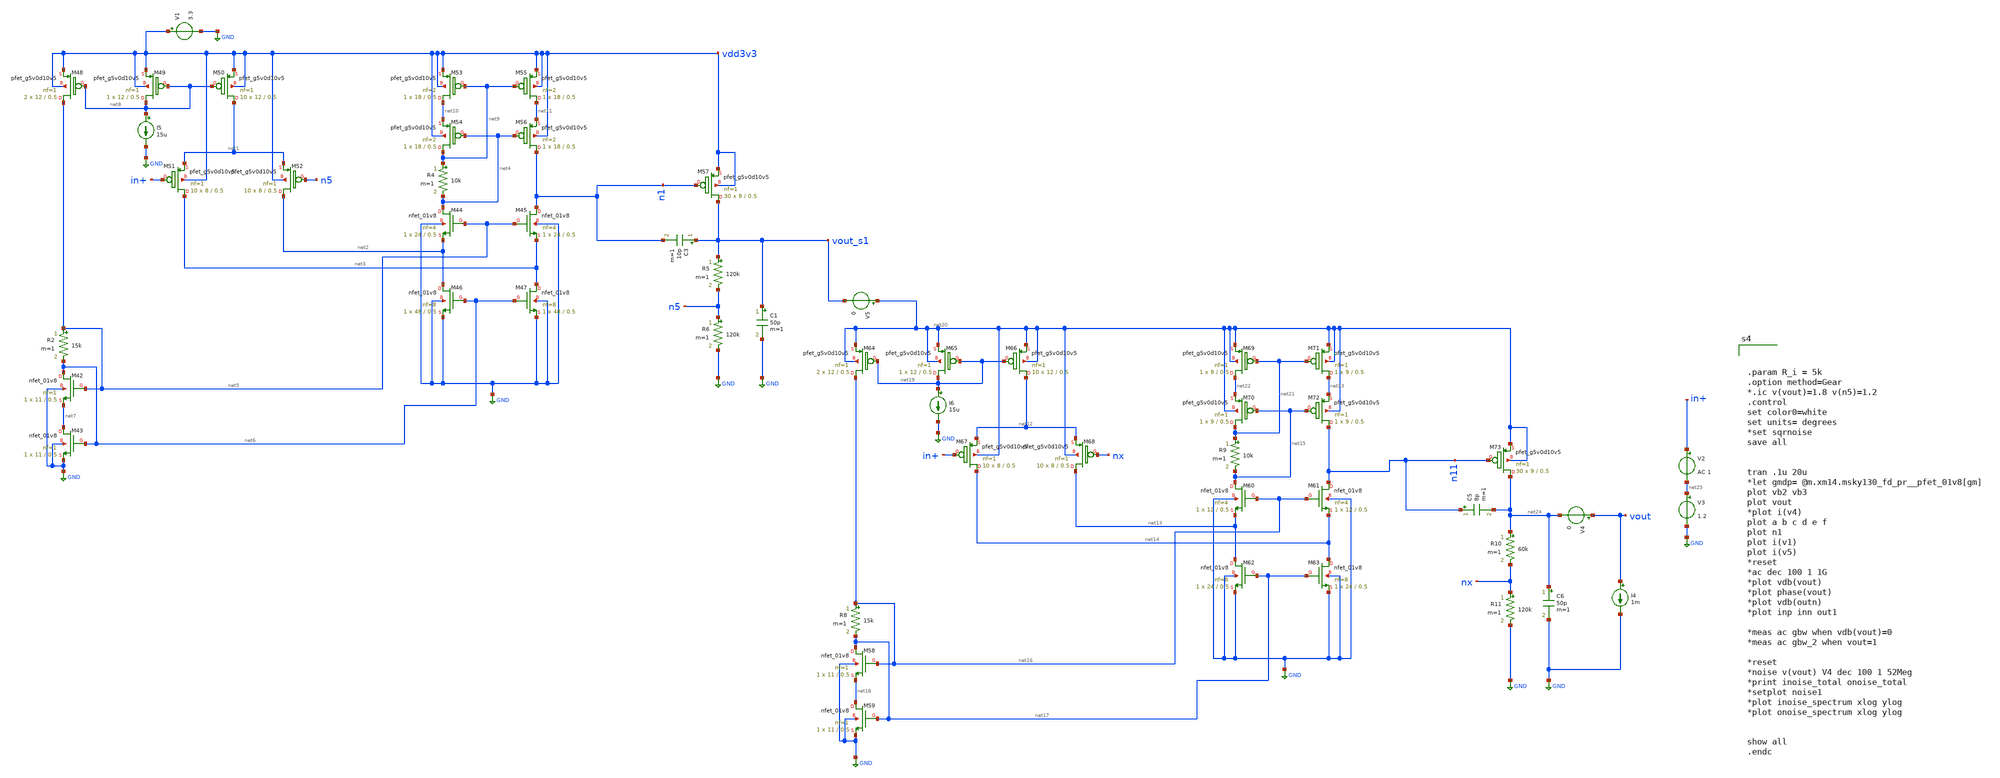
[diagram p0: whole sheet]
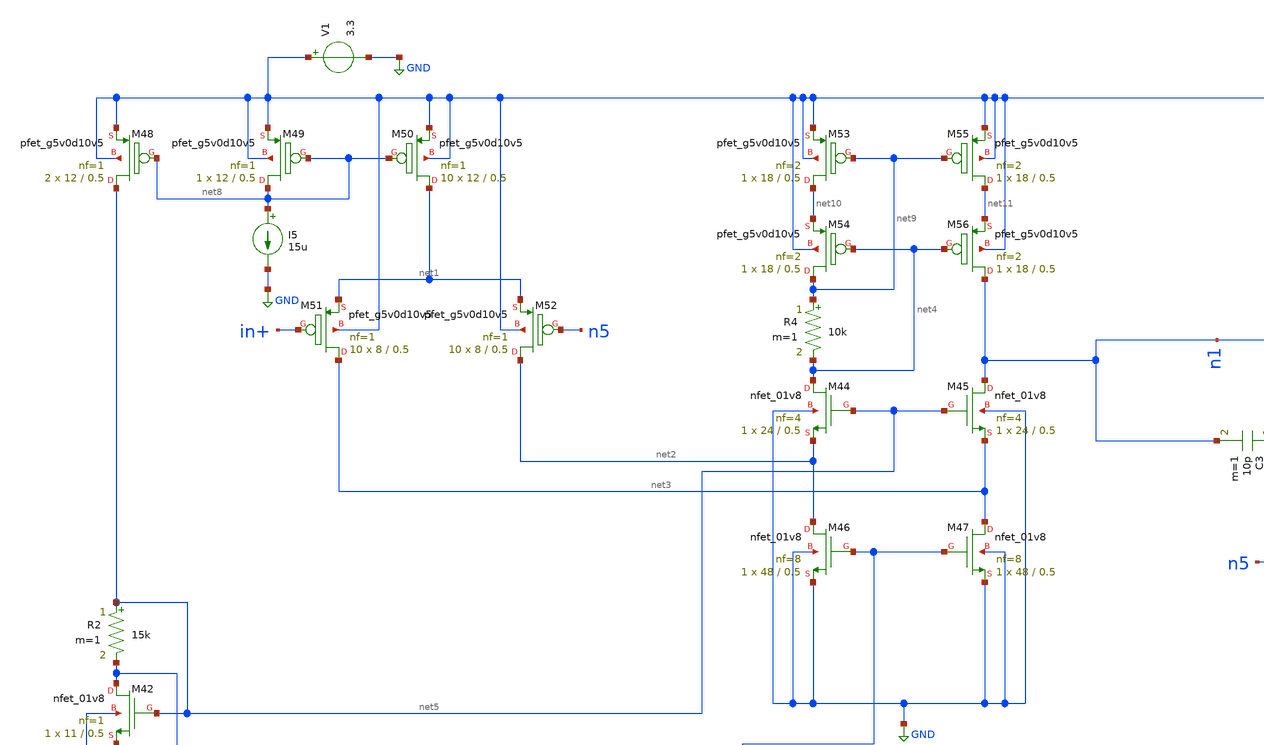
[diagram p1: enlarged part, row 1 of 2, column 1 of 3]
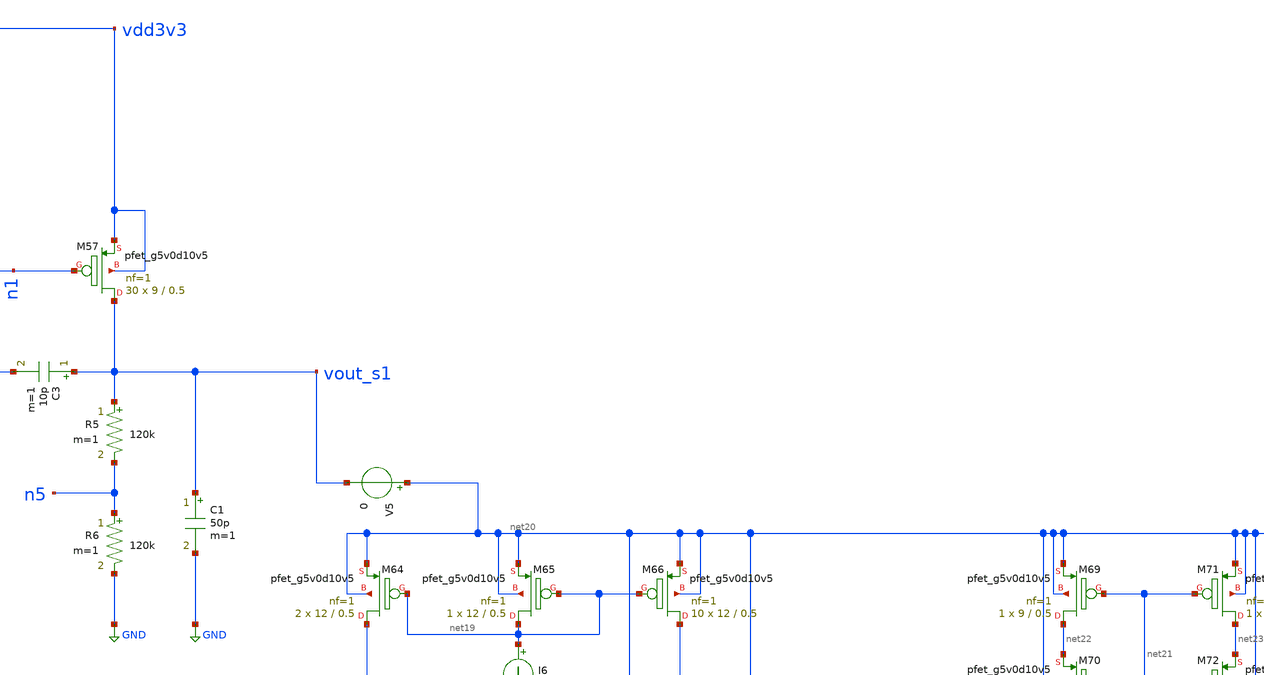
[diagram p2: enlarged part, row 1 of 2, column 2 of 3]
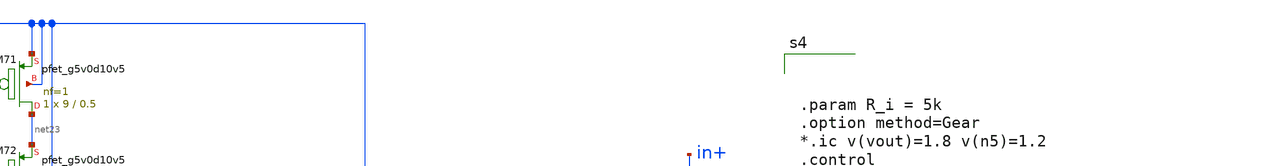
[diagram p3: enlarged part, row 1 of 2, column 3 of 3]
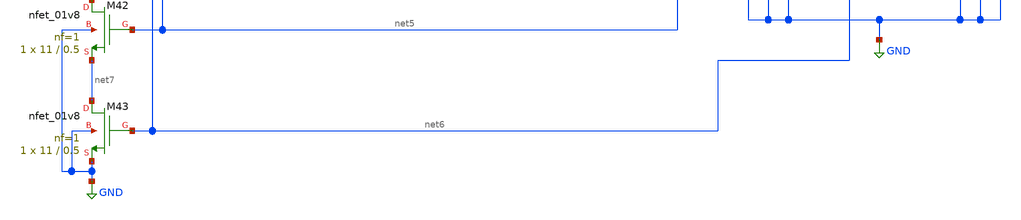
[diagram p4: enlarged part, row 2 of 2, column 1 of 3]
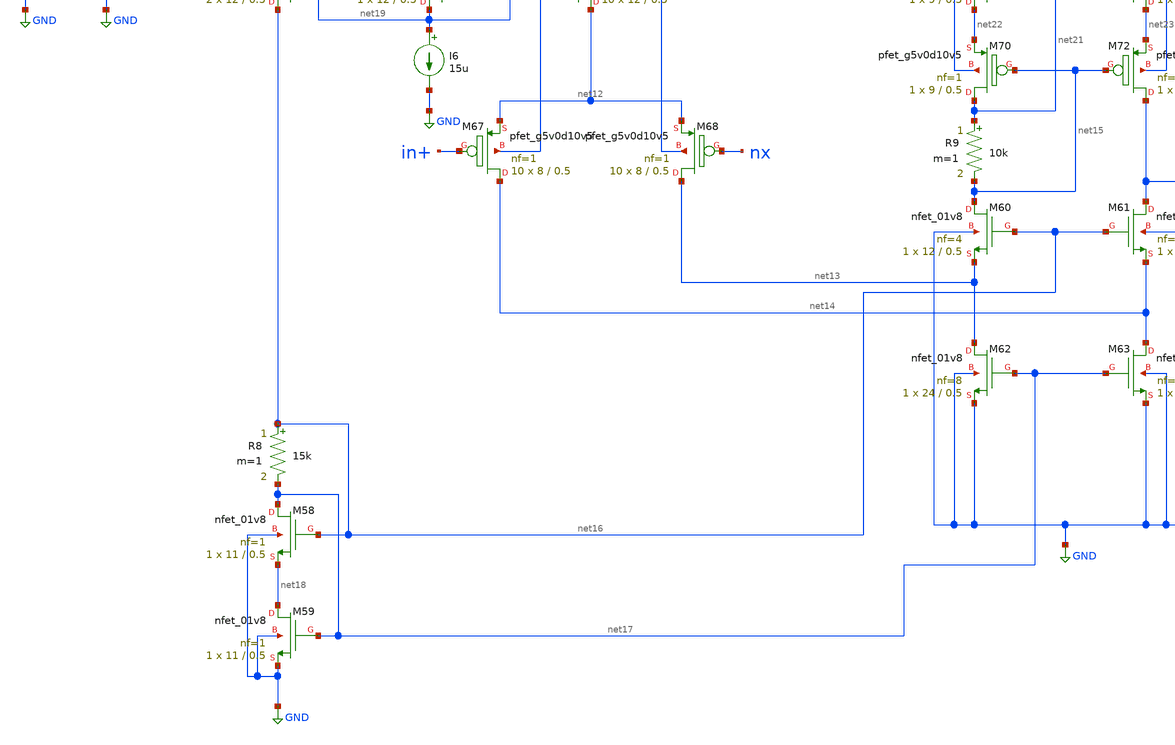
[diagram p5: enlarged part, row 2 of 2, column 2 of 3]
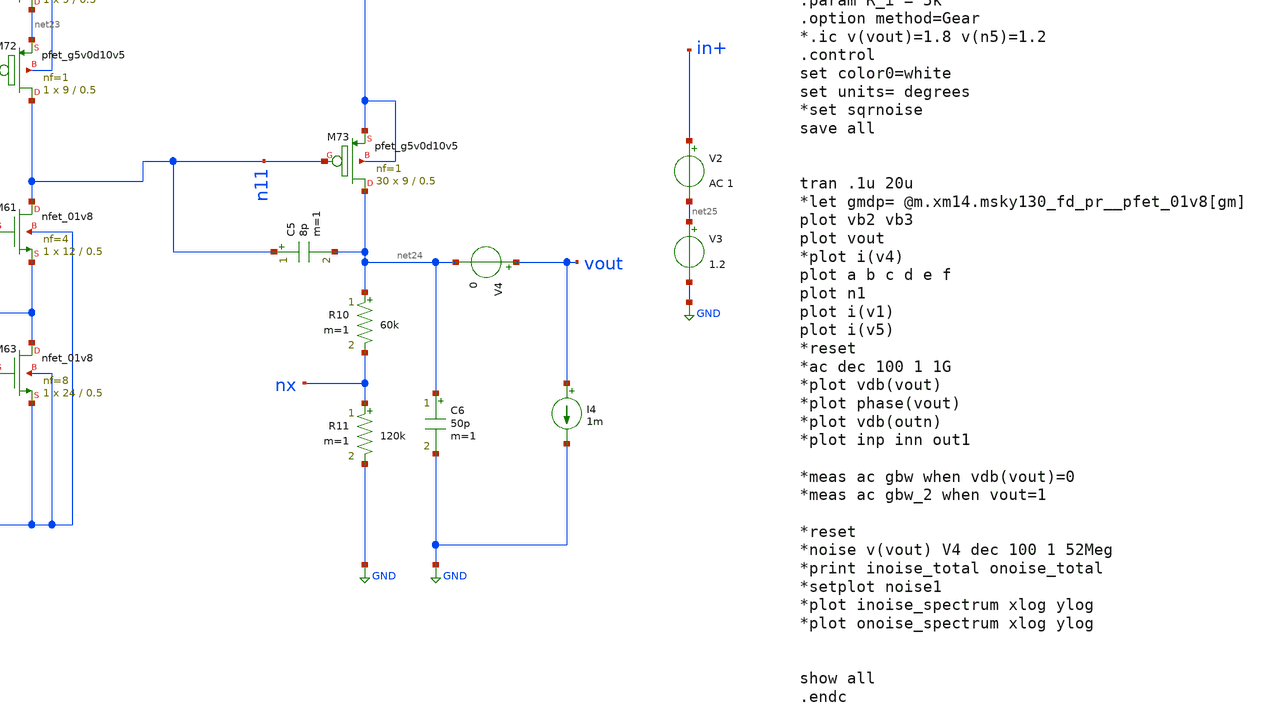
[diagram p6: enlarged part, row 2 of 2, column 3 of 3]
** sch_path: analog/analog_ldo/ceyda_src/cascade_ldo_tran.sch
**.subckt cascade_ldo_tran
R2 net5 net6 15k m=1
I5 net8 GND 15u
V1 vdd3v3 GND 3.3
R4 net9 net4 10k m=1
XM42 net6 net5 net7 GND sky130_fd_pr__nfet_01v8 L=0.5 W=11 nf=1 ad='int((nf+1)/2) * W/nf * 0.29' as='int((nf+2)/2) * W/nf * 0.29'
+ pd='2*int((nf+1)/2) * (W/nf + 0.29)' ps='2*int((nf+2)/2) * (W/nf + 0.29)' nrd='0.29 / W' nrs='0.29 / W'
+ sa=0 sb=0 sd=0 mult=1 m=1
XM43 net7 net6 GND GND sky130_fd_pr__nfet_01v8 L=0.5 W=11 nf=1 ad='int((nf+1)/2) * W/nf * 0.29' as='int((nf+2)/2) * W/nf * 0.29'
+ pd='2*int((nf+1)/2) * (W/nf + 0.29)' ps='2*int((nf+2)/2) * (W/nf + 0.29)' nrd='0.29 / W' nrs='0.29 / W'
+ sa=0 sb=0 sd=0 mult=1 m=1
XM44 net4 net5 net2 GND sky130_fd_pr__nfet_01v8 L=0.5 W=24 nf=4 ad='int((nf+1)/2) * W/nf * 0.29' as='int((nf+2)/2) * W/nf * 0.29'
+ pd='2*int((nf+1)/2) * (W/nf + 0.29)' ps='2*int((nf+2)/2) * (W/nf + 0.29)' nrd='0.29 / W' nrs='0.29 / W'
+ sa=0 sb=0 sd=0 mult=1 m=1
XM45 n1 net5 net3 GND sky130_fd_pr__nfet_01v8 L=0.5 W=24 nf=4 ad='int((nf+1)/2) * W/nf * 0.29' as='int((nf+2)/2) * W/nf * 0.29'
+ pd='2*int((nf+1)/2) * (W/nf + 0.29)' ps='2*int((nf+2)/2) * (W/nf + 0.29)' nrd='0.29 / W' nrs='0.29 / W'
+ sa=0 sb=0 sd=0 mult=1 m=1
XM46 net2 net6 GND GND sky130_fd_pr__nfet_01v8 L=0.5 W=48 nf=8 ad='int((nf+1)/2) * W/nf * 0.29' as='int((nf+2)/2) * W/nf * 0.29'
+ pd='2*int((nf+1)/2) * (W/nf + 0.29)' ps='2*int((nf+2)/2) * (W/nf + 0.29)' nrd='0.29 / W' nrs='0.29 / W'
+ sa=0 sb=0 sd=0 mult=1 m=1
XM47 net3 net6 GND GND sky130_fd_pr__nfet_01v8 L=0.5 W=48 nf=8 ad='int((nf+1)/2) * W/nf * 0.29' as='int((nf+2)/2) * W/nf * 0.29'
+ pd='2*int((nf+1)/2) * (W/nf + 0.29)' ps='2*int((nf+2)/2) * (W/nf + 0.29)' nrd='0.29 / W' nrs='0.29 / W'
+ sa=0 sb=0 sd=0 mult=1 m=1
XM48 net5 net8 vdd3v3 vdd3v3 sky130_fd_pr__pfet_g5v0d10v5 L=0.5 W=12 nf=1 ad='int((nf+1)/2) * W/nf * 0.29'
+ as='int((nf+2)/2) * W/nf * 0.29' pd='2*int((nf+1)/2) * (W/nf + 0.29)' ps='2*int((nf+2)/2) * (W/nf + 0.29)'
+ nrd='0.29 / W' nrs='0.29 / W' sa=0 sb=0 sd=0 mult=2 m=2
XM49 net8 net8 vdd3v3 vdd3v3 sky130_fd_pr__pfet_g5v0d10v5 L=0.5 W=12 nf=1 ad='int((nf+1)/2) * W/nf * 0.29'
+ as='int((nf+2)/2) * W/nf * 0.29' pd='2*int((nf+1)/2) * (W/nf + 0.29)' ps='2*int((nf+2)/2) * (W/nf + 0.29)'
+ nrd='0.29 / W' nrs='0.29 / W' sa=0 sb=0 sd=0 mult=1 m=1
XM50 net1 net8 vdd3v3 vdd3v3 sky130_fd_pr__pfet_g5v0d10v5 L=0.5 W=12 nf=1 ad='int((nf+1)/2) * W/nf * 0.29'
+ as='int((nf+2)/2) * W/nf * 0.29' pd='2*int((nf+1)/2) * (W/nf + 0.29)' ps='2*int((nf+2)/2) * (W/nf + 0.29)'
+ nrd='0.29 / W' nrs='0.29 / W' sa=0 sb=0 sd=0 mult=10 m=10
XM51 net3 in+ net1 vdd3v3 sky130_fd_pr__pfet_g5v0d10v5 L=0.5 W=8 nf=1 ad='int((nf+1)/2) * W/nf * 0.29'
+ as='int((nf+2)/2) * W/nf * 0.29' pd='2*int((nf+1)/2) * (W/nf + 0.29)' ps='2*int((nf+2)/2) * (W/nf + 0.29)'
+ nrd='0.29 / W' nrs='0.29 / W' sa=0 sb=0 sd=0 mult=10 m=10
XM52 net2 n5 net1 vdd3v3 sky130_fd_pr__pfet_g5v0d10v5 L=0.5 W=8 nf=1 ad='int((nf+1)/2) * W/nf * 0.29'
+ as='int((nf+2)/2) * W/nf * 0.29' pd='2*int((nf+1)/2) * (W/nf + 0.29)' ps='2*int((nf+2)/2) * (W/nf + 0.29)'
+ nrd='0.29 / W' nrs='0.29 / W' sa=0 sb=0 sd=0 mult=10 m=10
XM53 net10 net9 vdd3v3 vdd3v3 sky130_fd_pr__pfet_g5v0d10v5 L=0.5 W=18 nf=2 ad='int((nf+1)/2) * W/nf * 0.29'
+ as='int((nf+2)/2) * W/nf * 0.29' pd='2*int((nf+1)/2) * (W/nf + 0.29)' ps='2*int((nf+2)/2) * (W/nf + 0.29)'
+ nrd='0.29 / W' nrs='0.29 / W' sa=0 sb=0 sd=0 mult=1 m=1
XM54 net9 net4 net10 vdd3v3 sky130_fd_pr__pfet_g5v0d10v5 L=0.5 W=18 nf=2 ad='int((nf+1)/2) * W/nf * 0.29'
+ as='int((nf+2)/2) * W/nf * 0.29' pd='2*int((nf+1)/2) * (W/nf + 0.29)' ps='2*int((nf+2)/2) * (W/nf + 0.29)'
+ nrd='0.29 / W' nrs='0.29 / W' sa=0 sb=0 sd=0 mult=1 m=1
XM55 net11 net9 vdd3v3 vdd3v3 sky130_fd_pr__pfet_g5v0d10v5 L=0.5 W=18 nf=2 ad='int((nf+1)/2) * W/nf * 0.29'
+ as='int((nf+2)/2) * W/nf * 0.29' pd='2*int((nf+1)/2) * (W/nf + 0.29)' ps='2*int((nf+2)/2) * (W/nf + 0.29)'
+ nrd='0.29 / W' nrs='0.29 / W' sa=0 sb=0 sd=0 mult=1 m=1
XM56 n1 net4 net11 vdd3v3 sky130_fd_pr__pfet_g5v0d10v5 L=0.5 W=18 nf=2 ad='int((nf+1)/2) * W/nf * 0.29'
+ as='int((nf+2)/2) * W/nf * 0.29' pd='2*int((nf+1)/2) * (W/nf + 0.29)' ps='2*int((nf+2)/2) * (W/nf + 0.29)'
+ nrd='0.29 / W' nrs='0.29 / W' sa=0 sb=0 sd=0 mult=1 m=1
R5 vout_s1 n5 120k m=1
R6 n5 GND 120k m=1
XM57 vout_s1 n1 vdd3v3 vdd3v3 sky130_fd_pr__pfet_g5v0d10v5 L=0.5 W=9 nf=1 ad='int((nf+1)/2) * W/nf * 0.29'
+ as='int((nf+2)/2) * W/nf * 0.29' pd='2*int((nf+1)/2) * (W/nf + 0.29)' ps='2*int((nf+2)/2) * (W/nf + 0.29)'
+ nrd='0.29 / W' nrs='0.29 / W' sa=0 sb=0 sd=0 mult=30 m=30
R8 net16 net17 15k m=1
I6 net19 GND 15u
R9 net21 net15 10k m=1
XM58 net17 net16 net18 GND sky130_fd_pr__nfet_01v8 L=0.5 W=11 nf=1 ad='int((nf+1)/2) * W/nf * 0.29' as='int((nf+2)/2) * W/nf * 0.29'
+ pd='2*int((nf+1)/2) * (W/nf + 0.29)' ps='2*int((nf+2)/2) * (W/nf + 0.29)' nrd='0.29 / W' nrs='0.29 / W'
+ sa=0 sb=0 sd=0 mult=1 m=1
XM59 net18 net17 GND GND sky130_fd_pr__nfet_01v8 L=0.5 W=11 nf=1 ad='int((nf+1)/2) * W/nf * 0.29' as='int((nf+2)/2) * W/nf * 0.29'
+ pd='2*int((nf+1)/2) * (W/nf + 0.29)' ps='2*int((nf+2)/2) * (W/nf + 0.29)' nrd='0.29 / W' nrs='0.29 / W'
+ sa=0 sb=0 sd=0 mult=1 m=1
XM60 net15 net16 net13 GND sky130_fd_pr__nfet_01v8 L=0.5 W=12 nf=4 ad='int((nf+1)/2) * W/nf * 0.29' as='int((nf+2)/2) * W/nf * 0.29'
+ pd='2*int((nf+1)/2) * (W/nf + 0.29)' ps='2*int((nf+2)/2) * (W/nf + 0.29)' nrd='0.29 / W' nrs='0.29 / W'
+ sa=0 sb=0 sd=0 mult=1 m=1
XM61 n11 net16 net14 GND sky130_fd_pr__nfet_01v8 L=0.5 W=12 nf=4 ad='int((nf+1)/2) * W/nf * 0.29' as='int((nf+2)/2) * W/nf * 0.29'
+ pd='2*int((nf+1)/2) * (W/nf + 0.29)' ps='2*int((nf+2)/2) * (W/nf + 0.29)' nrd='0.29 / W' nrs='0.29 / W'
+ sa=0 sb=0 sd=0 mult=1 m=1
XM62 net13 net17 GND GND sky130_fd_pr__nfet_01v8 L=0.5 W=24 nf=8 ad='int((nf+1)/2) * W/nf * 0.29' as='int((nf+2)/2) * W/nf * 0.29'
+ pd='2*int((nf+1)/2) * (W/nf + 0.29)' ps='2*int((nf+2)/2) * (W/nf + 0.29)' nrd='0.29 / W' nrs='0.29 / W'
+ sa=0 sb=0 sd=0 mult=1 m=1
XM63 net14 net17 GND GND sky130_fd_pr__nfet_01v8 L=0.5 W=24 nf=8 ad='int((nf+1)/2) * W/nf * 0.29' as='int((nf+2)/2) * W/nf * 0.29'
+ pd='2*int((nf+1)/2) * (W/nf + 0.29)' ps='2*int((nf+2)/2) * (W/nf + 0.29)' nrd='0.29 / W' nrs='0.29 / W'
+ sa=0 sb=0 sd=0 mult=1 m=1
XM64 net16 net19 net20 net20 sky130_fd_pr__pfet_g5v0d10v5 L=0.5 W=12 nf=1 ad='int((nf+1)/2) * W/nf * 0.29'
+ as='int((nf+2)/2) * W/nf * 0.29' pd='2*int((nf+1)/2) * (W/nf + 0.29)' ps='2*int((nf+2)/2) * (W/nf + 0.29)'
+ nrd='0.29 / W' nrs='0.29 / W' sa=0 sb=0 sd=0 mult=2 m=2
XM65 net19 net19 net20 net20 sky130_fd_pr__pfet_g5v0d10v5 L=0.5 W=12 nf=1 ad='int((nf+1)/2) * W/nf * 0.29'
+ as='int((nf+2)/2) * W/nf * 0.29' pd='2*int((nf+1)/2) * (W/nf + 0.29)' ps='2*int((nf+2)/2) * (W/nf + 0.29)'
+ nrd='0.29 / W' nrs='0.29 / W' sa=0 sb=0 sd=0 mult=1 m=1
XM66 net12 net19 net20 net20 sky130_fd_pr__pfet_g5v0d10v5 L=0.5 W=12 nf=1 ad='int((nf+1)/2) * W/nf * 0.29'
+ as='int((nf+2)/2) * W/nf * 0.29' pd='2*int((nf+1)/2) * (W/nf + 0.29)' ps='2*int((nf+2)/2) * (W/nf + 0.29)'
+ nrd='0.29 / W' nrs='0.29 / W' sa=0 sb=0 sd=0 mult=10 m=10
XM67 net14 in+ net12 net20 sky130_fd_pr__pfet_g5v0d10v5 L=0.5 W=8 nf=1 ad='int((nf+1)/2) * W/nf * 0.29'
+ as='int((nf+2)/2) * W/nf * 0.29' pd='2*int((nf+1)/2) * (W/nf + 0.29)' ps='2*int((nf+2)/2) * (W/nf + 0.29)'
+ nrd='0.29 / W' nrs='0.29 / W' sa=0 sb=0 sd=0 mult=10 m=10
XM68 net13 nx net12 net20 sky130_fd_pr__pfet_g5v0d10v5 L=0.5 W=8 nf=1 ad='int((nf+1)/2) * W/nf * 0.29'
+ as='int((nf+2)/2) * W/nf * 0.29' pd='2*int((nf+1)/2) * (W/nf + 0.29)' ps='2*int((nf+2)/2) * (W/nf + 0.29)'
+ nrd='0.29 / W' nrs='0.29 / W' sa=0 sb=0 sd=0 mult=10 m=10
XM69 net22 net21 net20 net20 sky130_fd_pr__pfet_g5v0d10v5 L=0.5 W=9 nf=1 ad='int((nf+1)/2) * W/nf * 0.29'
+ as='int((nf+2)/2) * W/nf * 0.29' pd='2*int((nf+1)/2) * (W/nf + 0.29)' ps='2*int((nf+2)/2) * (W/nf + 0.29)'
+ nrd='0.29 / W' nrs='0.29 / W' sa=0 sb=0 sd=0 mult=1 m=1
XM70 net21 net15 net22 net20 sky130_fd_pr__pfet_g5v0d10v5 L=0.5 W=9 nf=1 ad='int((nf+1)/2) * W/nf * 0.29'
+ as='int((nf+2)/2) * W/nf * 0.29' pd='2*int((nf+1)/2) * (W/nf + 0.29)' ps='2*int((nf+2)/2) * (W/nf + 0.29)'
+ nrd='0.29 / W' nrs='0.29 / W' sa=0 sb=0 sd=0 mult=1 m=1
XM71 net23 net21 net20 net20 sky130_fd_pr__pfet_g5v0d10v5 L=0.5 W=9 nf=1 ad='int((nf+1)/2) * W/nf * 0.29'
+ as='int((nf+2)/2) * W/nf * 0.29' pd='2*int((nf+1)/2) * (W/nf + 0.29)' ps='2*int((nf+2)/2) * (W/nf + 0.29)'
+ nrd='0.29 / W' nrs='0.29 / W' sa=0 sb=0 sd=0 mult=1 m=1
XM72 n11 net15 net23 net20 sky130_fd_pr__pfet_g5v0d10v5 L=0.5 W=9 nf=1 ad='int((nf+1)/2) * W/nf * 0.29'
+ as='int((nf+2)/2) * W/nf * 0.29' pd='2*int((nf+1)/2) * (W/nf + 0.29)' ps='2*int((nf+2)/2) * (W/nf + 0.29)'
+ nrd='0.29 / W' nrs='0.29 / W' sa=0 sb=0 sd=0 mult=1 m=1
R10 net24 nx 60k m=1
R11 nx GND 120k m=1
XM73 net24 n11 net20 net20 sky130_fd_pr__pfet_g5v0d10v5 L=0.5 W=9 nf=1 ad='int((nf+1)/2) * W/nf * 0.29'
+ as='int((nf+2)/2) * W/nf * 0.29' pd='2*int((nf+1)/2) * (W/nf + 0.29)' ps='2*int((nf+2)/2) * (W/nf + 0.29)'
+ nrd='0.29 / W' nrs='0.29 / W' sa=0 sb=0 sd=0 mult=30 m=30
C5 n11 net24 8p m=1
C6 net24 GND 50p m=1
V5 net20 vout_s1 0
C3 vout_s1 n1 10p m=1
V3 net25 GND 1.2
V2 in+ net25 AC 1
C1 vout_s1 GND 50p m=1
I4 vout GND 1m
V4 vout net24 0
**** begin user architecture code

** opencircuitdesign pdks install
.lib $::SKYWATER_MODELS/sky130.lib.spice tt





.param R_i = 5k
.option method=Gear
*.ic v(vout)=1.8 v(n5)=1.2
.control
set color0=white
set units= degrees
*set sqrnoise
save all


tran .1u 20u
*let gmdp= @m.xm14.msky130_fd_pr__pfet_01v8[gm]
plot vb2 vb3
plot vout
*plot i(v4)
plot a b c d e f
plot n1
plot i(v1)
plot i(v5)
*reset
*ac dec 100 1 1G
*plot vdb(vout)
*plot phase(vout)
*plot vdb(outn)
*plot inp inn out1

*meas ac gbw when vdb(vout)=0
*meas ac gbw_2 when vout=1

*reset
*noise v(vout) V4 dec 100 1 52Meg
*print inoise_total onoise_total
*setplot noise1
*plot inoise_spectrum xlog ylog
*plot onoise_spectrum xlog ylog


show all
.endc


**** end user architecture code
**.ends
.GLOBAL GND
.end
